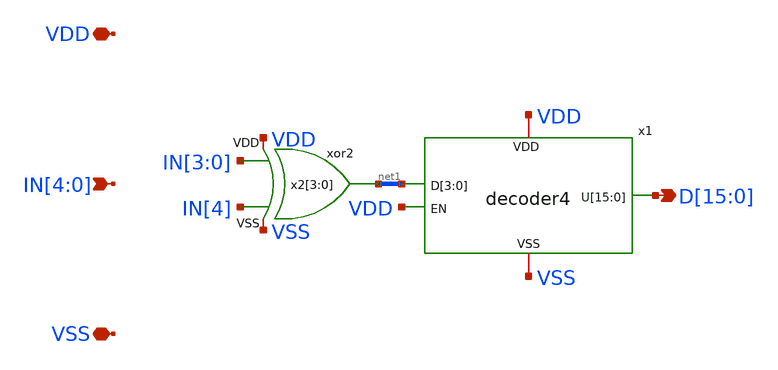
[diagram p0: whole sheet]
** sch_path: xschem/lsb_decoder.sch
**.subckt lsb_decoder VDD VSS IN[4],IN[3],IN[2],IN[1],IN[0]
*+ D[15],D[14],D[13],D[12],D[11],D[10],D[9],D[8],D[7],D[6],D[5],D[4],D[3],D[2],D[1],D[0]
*.iopin VDD
*.iopin VSS
*.ipin IN[4],IN[3],IN[2],IN[1],IN[0]
*.opin D[15],D[14],D[13],D[12],D[11],D[10],D[9],D[8],D[7],D[6],D[5],D[4],D[3],D[2],D[1],D[0]
x1 VDD net1[3] net1[2] net1[1] net1[0] D[15] D[14] D[13] D[12] D[11] D[10] D[9] D[8] D[7] D[6] D[5]
+ D[4] D[3] D[2] D[1] D[0] VSS VDD decoder4
x2[3] VDD IN[3] net1[3] IN[4] VSS xor2
x2[2] VDD IN[2] net1[2] IN[4] VSS xor2
x2[1] VDD IN[1] net1[1] IN[4] VSS xor2
x2[0] VDD IN[0] net1[0] IN[4] VSS xor2
**.ends
.end
